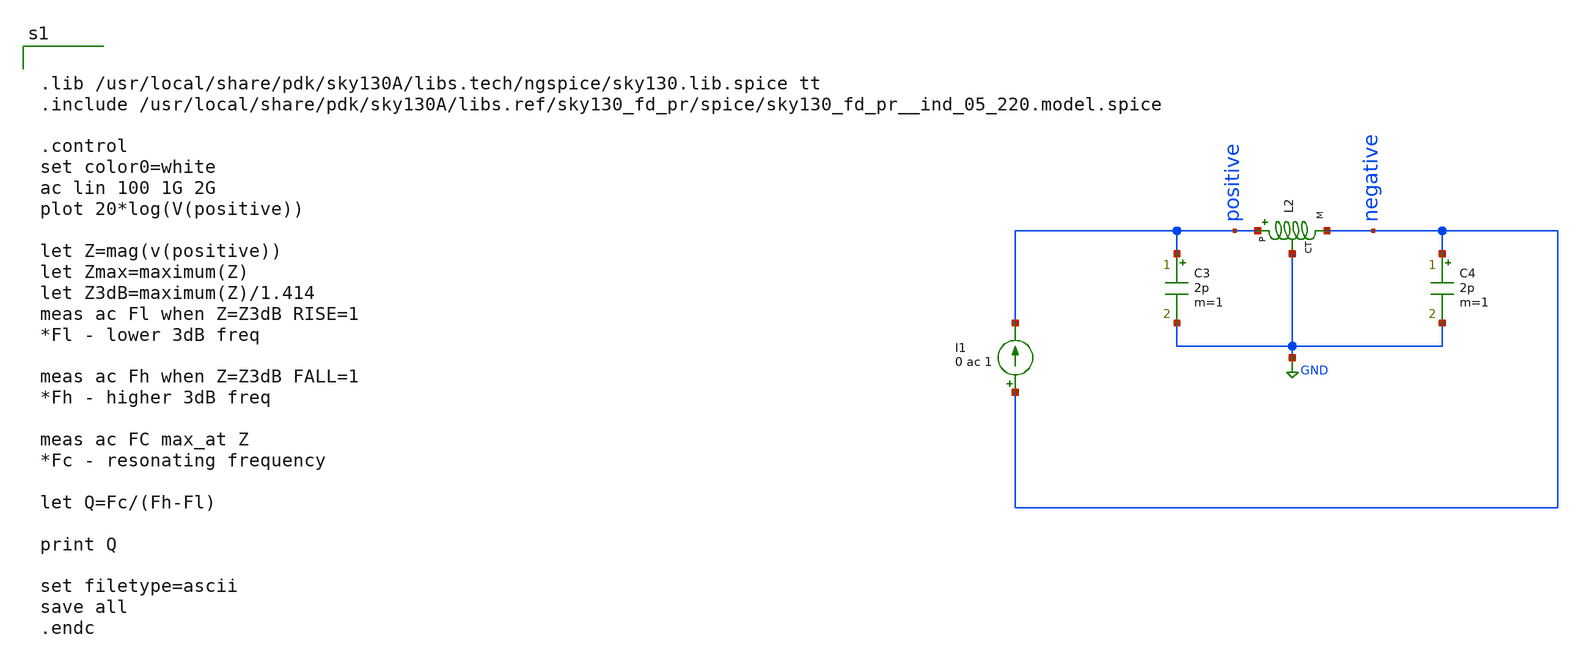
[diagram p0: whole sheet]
** sch_path: ind_Q_meas/ind_4p96_Q_measurement.sch
**.subckt ind_4p96_Q_measurement
XL2 positive negative GND GND sky130_fd_pr__ind_05_220
C3 positive GND 2p m=1
C4 negative GND 2p m=1
I1 negative positive 0 ac 1
**** begin user architecture code


.lib /usr/local/share/pdk/sky130A/libs.tech/ngspice/sky130.lib.spice tt
.include /usr/local/share/pdk/sky130A/libs.ref/sky130_fd_pr/spice/sky130_fd_pr__ind_05_220.model.spice

.control
set color0=white
ac lin 100 1G 2G
plot 20*log(V(positive))

let Z=mag(v(positive))
let Zmax=maximum(Z)
let Z3dB=maximum(Z)/1.414
meas ac Fl when Z=Z3dB RISE=1
*Fl - lower 3dB freq

meas ac Fh when Z=Z3dB FALL=1
*Fh - higher 3dB freq

meas ac FC max_at Z
*Fc - resonating frequency

let Q=Fc/(Fh-Fl)

print Q

set filetype=ascii
save all
.endc


**** end user architecture code
**.ends
.GLOBAL GND
.end
